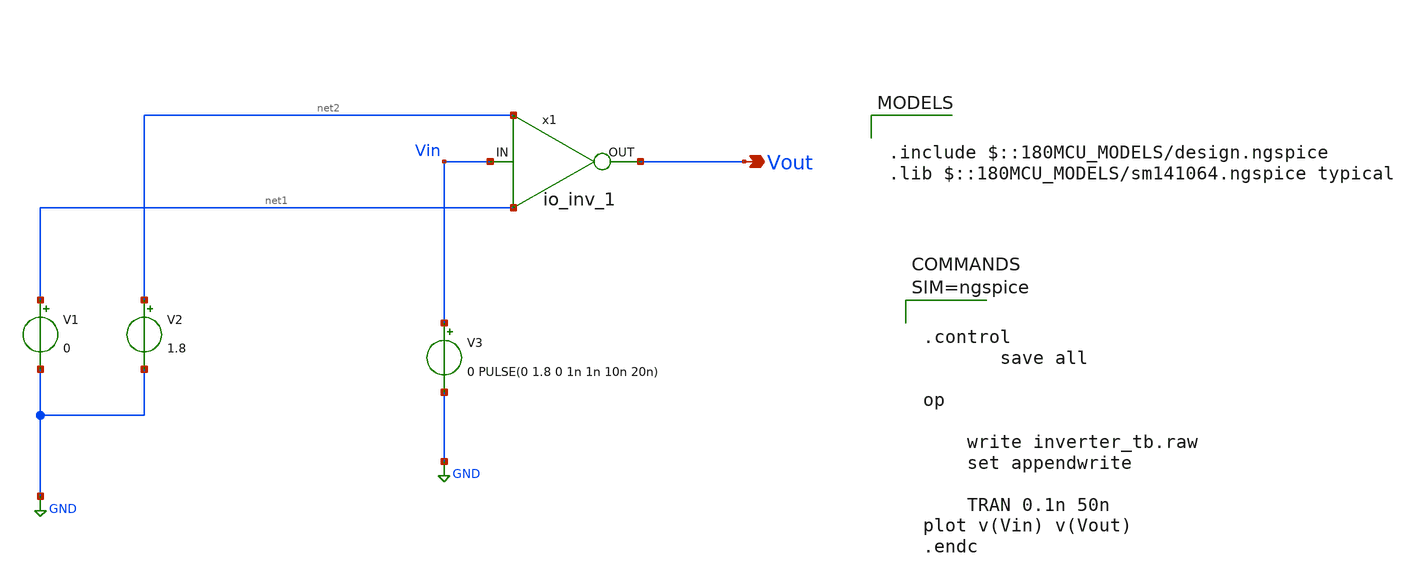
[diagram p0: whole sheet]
** sch_path: xschem/io_inv_1_tb.sch
* Copyright 2023 David Mitchell Bailey
* Licensed under the Apache License, Version 2.0 (the "License");
* you may not use this file except in compliance with the License.
* You may obtain a copy of the License at
* https://www.apache.org/licenses/LICENSE-2.0
* Unless required by applicable law or agreed to in writing, software
* distributed under the License is distributed on an "AS IS" BASIS,
* WITHOUT WARRANTIES OR CONDITIONS OF ANY KIND, either express or implied.
* See the License for the specific language governing permissions and
* limitations under the License.
**.subckt io_inv_1_tb Vout
*.opin Vout
x1 Vin Vout net2 net1 io_inv_1
V1 net1 GND 0
V2 net2 GND 1.8
V3 Vin GND 0 PULSE(0 1.8 0 1n 1n 10n 20n)
**** begin user architecture code

.include $::180MCU_MODELS/design.ngspice
.lib $::180MCU_MODELS/sm141064.ngspice typical




.control
	   save all

op

    write inverter_tb.raw
    set appendwrite

	TRAN 0.1n 50n
plot v(Vin) v(Vout)
.endc




**** end user architecture code
**.ends
.GLOBAL GND
.end
